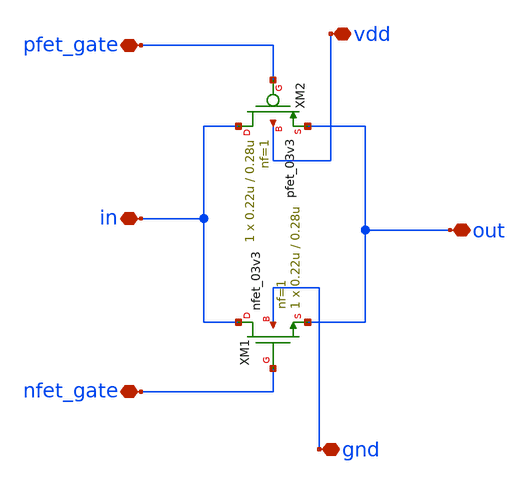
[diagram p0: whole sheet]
** sch_path: designs/schematics/mux2x1_transmission_gate/mux_tg.sch
**.subckt mux_tg vdd gnd out in pfet_gate nfet_gate
*.iopin vdd
*.iopin gnd
*.iopin out
*.iopin in
*.iopin pfet_gate
*.iopin nfet_gate
XM1 in nfet_gate out gnd nfet_03v3 L=0.28u W=0.22u nf=1 ad='int((nf+1)/2) * W/nf * 0.18u' as='int((nf+2)/2) * W/nf * 0.18u'
+ pd='2*int((nf+1)/2) * (W/nf + 0.18u)' ps='2*int((nf+2)/2) * (W/nf + 0.18u)' nrd='0.18u / W' nrs='0.18u / W'
+ sa=0 sb=0 sd=0 m=1
XM2 in pfet_gate out vdd pfet_03v3 L=0.28u W=0.22u nf=1 ad='int((nf+1)/2) * W/nf * 0.18u' as='int((nf+2)/2) * W/nf * 0.18u'
+ pd='2*int((nf+1)/2) * (W/nf + 0.18u)' ps='2*int((nf+2)/2) * (W/nf + 0.18u)' nrd='0.18u / W' nrs='0.18u / W'
+ sa=0 sb=0 sd=0 m=1
**.ends
.end
